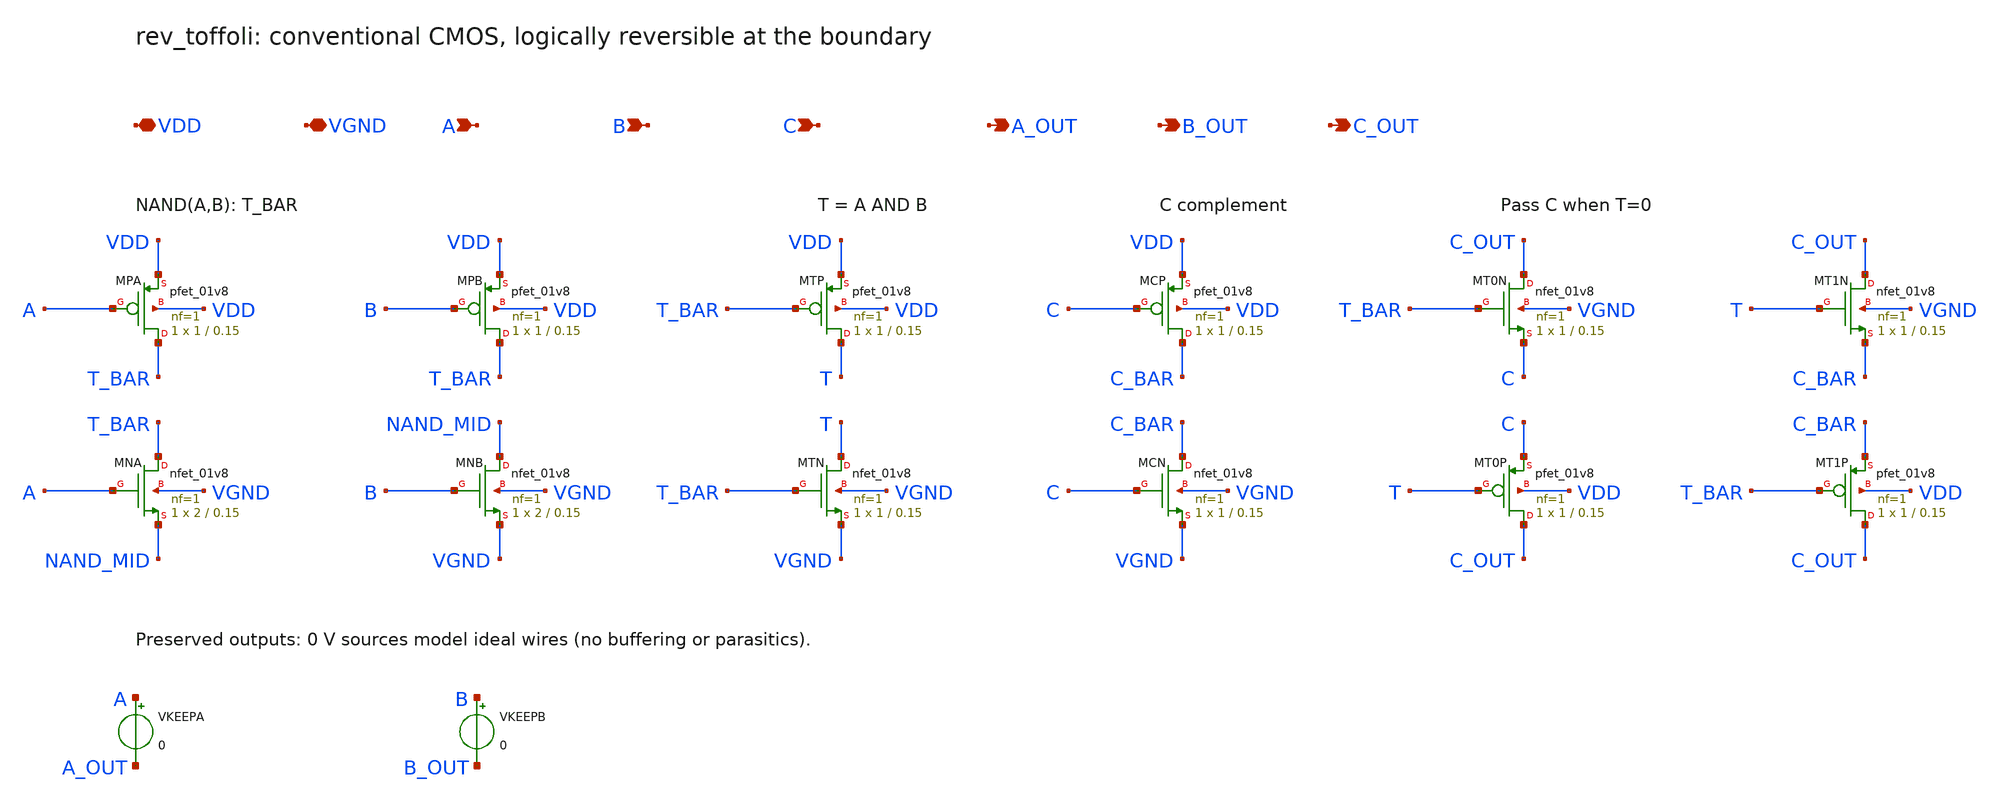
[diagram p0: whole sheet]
** sch_path: src/reversible_stdcells/rev_toffoli/rev_toffoli.sch
**.subckt rev_toffoli VDD VGND A B C A_OUT B_OUT C_OUT
*.iopin VDD
*.iopin VGND
*.ipin A
*.ipin B
*.ipin C
*.opin A_OUT
*.opin B_OUT
*.opin C_OUT
XMPA T_BAR A VDD VDD sky130_fd_pr__pfet_01v8 L=0.15 W=1 nf=1 ad=0.29 as=0.29 pd=2.58 ps=2.58
+ nrd=0.29 nrs=0.29 sa=0 sb=0 sd=0 mult=1 m=1
XMPB T_BAR B VDD VDD sky130_fd_pr__pfet_01v8 L=0.15 W=1 nf=1 ad=0.29 as=0.29 pd=2.58 ps=2.58
+ nrd=0.29 nrs=0.29 sa=0 sb=0 sd=0 mult=1 m=1
XMNA T_BAR A NAND_MID VGND sky130_fd_pr__nfet_01v8 L=0.15 W=2 nf=1 ad=0.58 as=0.58 pd=4.58 ps=4.58
+ nrd=0.145 nrs=0.145 sa=0 sb=0 sd=0 mult=1 m=1
XMNB NAND_MID B VGND VGND sky130_fd_pr__nfet_01v8 L=0.15 W=2 nf=1 ad=0.58 as=0.58 pd=4.58 ps=4.58
+ nrd=0.145 nrs=0.145 sa=0 sb=0 sd=0 mult=1 m=1
XMTP T T_BAR VDD VDD sky130_fd_pr__pfet_01v8 L=0.15 W=1 nf=1 ad=0.29 as=0.29 pd=2.58 ps=2.58
+ nrd=0.29 nrs=0.29 sa=0 sb=0 sd=0 mult=1 m=1
XMTN T T_BAR VGND VGND sky130_fd_pr__nfet_01v8 L=0.15 W=1 nf=1 ad=0.29 as=0.29 pd=2.58 ps=2.58
+ nrd=0.29 nrs=0.29 sa=0 sb=0 sd=0 mult=1 m=1
XMCP C_BAR C VDD VDD sky130_fd_pr__pfet_01v8 L=0.15 W=1 nf=1 ad=0.29 as=0.29 pd=2.58 ps=2.58
+ nrd=0.29 nrs=0.29 sa=0 sb=0 sd=0 mult=1 m=1
XMCN C_BAR C VGND VGND sky130_fd_pr__nfet_01v8 L=0.15 W=1 nf=1 ad=0.29 as=0.29 pd=2.58 ps=2.58
+ nrd=0.29 nrs=0.29 sa=0 sb=0 sd=0 mult=1 m=1
XMT0N C_OUT T_BAR C VGND sky130_fd_pr__nfet_01v8 L=0.15 W=1 nf=1 ad=0.29 as=0.29 pd=2.58 ps=2.58
+ nrd=0.29 nrs=0.29 sa=0 sb=0 sd=0 mult=1 m=1
XMT0P C_OUT T C VDD sky130_fd_pr__pfet_01v8 L=0.15 W=1 nf=1 ad=0.29 as=0.29 pd=2.58 ps=2.58 nrd=0.29
+ nrs=0.29 sa=0 sb=0 sd=0 mult=1 m=1
XMT1N C_OUT T C_BAR VGND sky130_fd_pr__nfet_01v8 L=0.15 W=1 nf=1 ad=0.29 as=0.29 pd=2.58 ps=2.58
+ nrd=0.29 nrs=0.29 sa=0 sb=0 sd=0 mult=1 m=1
XMT1P C_OUT T_BAR C_BAR VDD sky130_fd_pr__pfet_01v8 L=0.15 W=1 nf=1 ad=0.29 as=0.29 pd=2.58 ps=2.58
+ nrd=0.29 nrs=0.29 sa=0 sb=0 sd=0 mult=1 m=1
VKEEPA A A_OUT 0
VKEEPB B B_OUT 0
**.ends
.end
